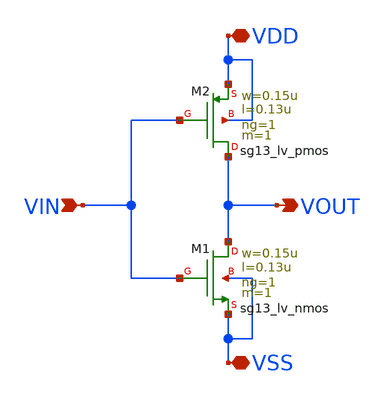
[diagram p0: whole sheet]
** sch_path: CDR4176-main/schematic/xschem/inv_CDR/inv_CDR.sch
**.subckt inv_CDR VDD VSS VOUT VIN
*.iopin VDD
*.iopin VSS
*.opin VOUT
*.ipin VIN
XM2 VOUT VIN VDD VDD sg13_lv_pmos w=0.15u l=0.13u ng=1 m=1 mm_ok=1
XM1 VOUT VIN VSS VSS sg13_lv_nmos w=0.15u l=0.13u ng=1 m=1 mm_ok=1
**.ends
.end
